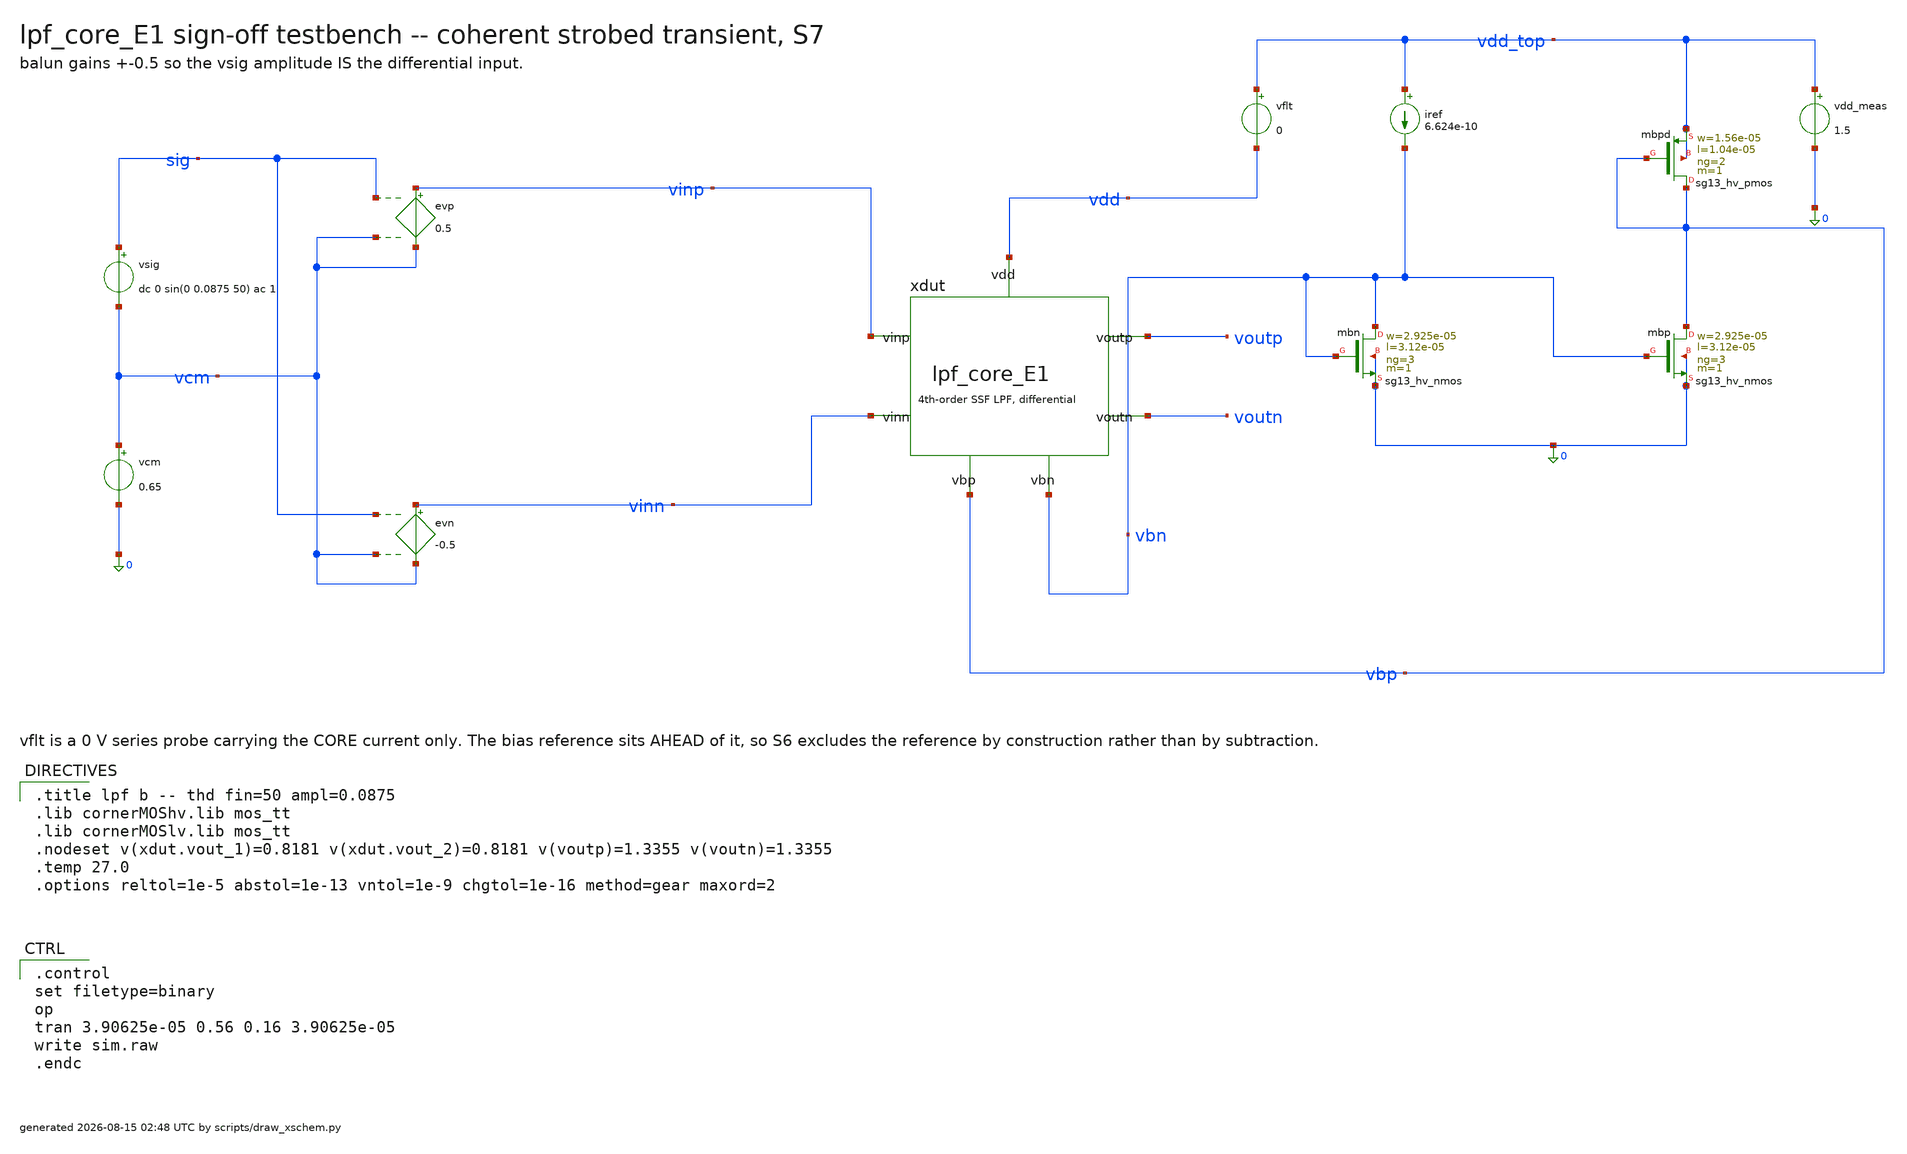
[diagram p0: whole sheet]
** sch_path: signoff/pre-pvt/E1-prev/lpf_tb_E1_thd.sch
**.subckt lpf_tb_E1_thd
vsig sig vcm dc 0 sin(0 0.0875 50) ac 1
vcm vcm 0 0.65
evp vinp vcm sig vcm 0.5
evn vinn vcm sig vcm -0.5
xdut vinp vinn voutp voutn vbn vbp vdd lpf_core_E1
vflt vdd_top vdd 0
vdd_meas vdd_top 0 1.5
iref vdd_top vbn 6.624e-10
Xmbn vbn vbn 0 0 sg13_hv_nmos w=2.925e-05 l=3.12e-05 ng=3 m=1 mm_ok=1
Xmbp vbp vbn 0 0 sg13_hv_nmos w=2.925e-05 l=3.12e-05 ng=3 m=1 mm_ok=1
Xmbpd vbp vbp vdd_top vdd_top sg13_hv_pmos w=1.56e-05 l=1.04e-05 ng=2 m=1 mm_ok=1
**** begin user architecture code

.title lpf b -- thd fin=50 ampl=0.0875
.lib cornerMOShv.lib mos_tt
.lib cornerMOSlv.lib mos_tt
.nodeset v(xdut.vout_1)=0.8181 v(xdut.vout_2)=0.8181 v(voutp)=1.3355 v(voutn)=1.3355
.temp 27.0
.options reltol=1e-5 abstol=1e-13 vntol=1e-9 chgtol=1e-16 method=gear maxord=2


.control
set filetype=binary
op
tran 3.90625e-05 0.56 0.16 3.90625e-05
write sim.raw
.endc

**** end user architecture code
**.ends

* expanding   symbol:  lpf_core_E1.sym # of pins=7
** sym_path: signoff/E1-prev/lpf_core_E1.sym
** sch_path: signoff/E1-prev/lpf_core_E1.sch
.subckt lpf_core_E1 vinp vinn voutp voutn vbn vbp vdd
*.ipin vinp
*.ipin vinn
*.opin voutp
*.opin voutn
*.ipin vdd
*.ipin vbn
*.ipin vbp
Xm2 net2 vinp vout_1 vout_1 sg13_lv_pmos w=1.56e-05 l=1.04e-05 ng=1 m=1 mm_ok=1
Xm5 net3 vinn vout_2 vout_2 sg13_lv_pmos w=1.56e-05 l=1.04e-05 ng=1 m=1 mm_ok=1
Xm4 vout_1 net2 0 0 sg13_hv_nmos w=7.8e-06 l=5.2e-06 ng=1 m=1 mm_ok=1
Xm8 vout_2 net3 0 0 sg13_hv_nmos w=7.8e-06 l=5.2e-06 ng=1 m=1 mm_ok=1
Xm9 net2 vbn 0 0 sg13_hv_nmos w=2.925e-05 l=3.12e-05 ng=1 m=1 mm_ok=1
Xm10 net3 vbn 0 0 sg13_hv_nmos w=2.925e-05 l=3.12e-05 ng=1 m=1 mm_ok=1
Xmst vout_1 vbn net4 net4 sg13_hv_pmos w=2.5896e-07 l=4.368e-05 ng=1 m=1 mm_ok=1
Xmstn vout_2 vbn net1 net1 sg13_hv_pmos w=2.5896e-07 l=4.368e-05 ng=1 m=1 mm_ok=1
Xm0 net4 vout_1 voutp voutp sg13_hv_pmos w=1.56e-05 l=1.04e-05 ng=1 m=1 mm_ok=1
Xm1 net1 vout_2 voutn voutn sg13_hv_pmos w=1.56e-05 l=1.04e-05 ng=1 m=1 mm_ok=1
Xm14 voutp net4 vdd vdd sg13_lv_pmos w=1.29324e-06 l=6.24e-05 ng=1 m=1 mm_ok=1
Xm15 voutn net1 vdd vdd sg13_lv_pmos w=1.29324e-06 l=6.24e-05 ng=1 m=1 mm_ok=1
c13 net2 vout_1 8.53159e-12 m=1
c17 net3 vout_2 8.53159e-12 m=1
c19 vout_2 vout_1 3.22133e-11 m=1
c1 voutp net4 8.17985e-11 m=1
c10 voutn net1 8.17985e-11 m=1
c12 voutn voutp 1.64735e-11 m=1
.ends

.end
